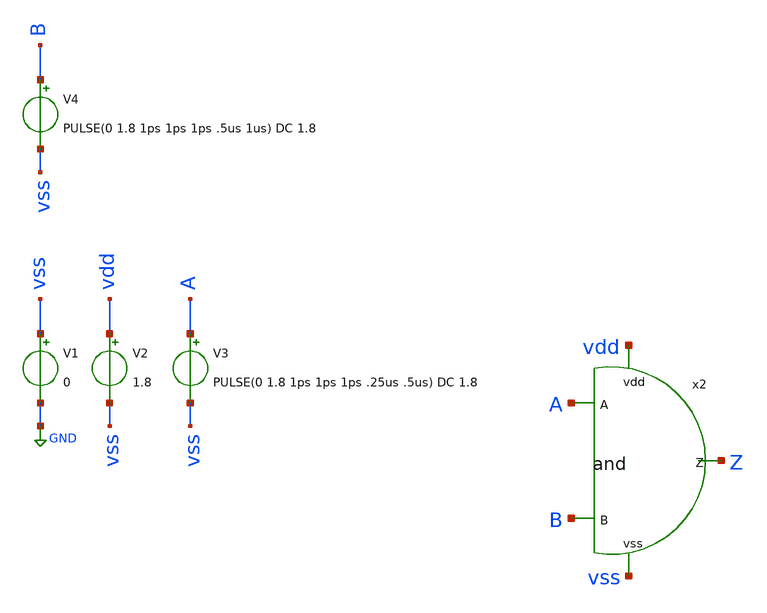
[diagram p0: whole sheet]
** sch_path: track_vlsi/somoza/sch/tb_and.sch
**.subckt tb_and
V1 vss GND 0
V2 vdd vss 1.8
V3 A vss PULSE(0 1.8 1ps 1ps 1ps .25us .5us) DC 1.8
V4 B vss PULSE(0 1.8 1ps 1ps 1ps .5us 1us) DC 1.8
x2 vdd A Z B vss and
**** begin user architecture code



* Parametros del circuito

.options TEMP = 27.0

* Include
.lib /home/eamta/skywater/skywater-pdk/libraries/sky130_fd_pr_ngspice/latest/models/corners/sky130.lib TT

* Signals to SAVE
*.save all
*+ @M.x1.XM1.msky130_fd_pr__nfet_01v8[id] @M.x1.XM1.msky130_fd_pr__nfet_01v8[gm]
*+ @M.x1.XM2.msky130_fd_pr__pfet_01v8[id] @M.x1.XM2.msky130_fd_pr__pfet_01v8[gm]

* Simulation
.control
  tran .001u 1us
  setplot tran1
  plot v(A)
  plot v(B)
  plot v(Z)
  write tb_and_tran.raw

.endc

.end


**** end user architecture code
**.ends

* expanding   symbol:  and/and.sym # of pins=5
** sym_path: track_vlsi/somoza/sch/and.sym
** sch_path: track_vlsi/somoza/sch/and.sch
.subckt and vdd A Z B vss
*.ipin A
*.ipin B
*.ipin vdd
*.opin Z
*.ipin vss
XM2 net1 A net2 vss sky130_fd_pr__nfet_01v8 L=0.15 W=0.9 nf=1 ad='int((nf+1)/2) * W/nf * 0.29' as='int((nf+2)/2) * W/nf * 0.29'
+ pd='2*int((nf+1)/2) * (W/nf + 0.29)' ps='2*int((nf+2)/2) * (W/nf + 0.29)' nrd='0.29 / W' nrs='0.29 / W'
+ sa=0 sb=0 sd=0 mult=1 m=1
XM3 net2 B vss vss sky130_fd_pr__nfet_01v8 L=0.15 W=0.9 nf=1 ad='int((nf+1)/2) * W/nf * 0.29' as='int((nf+2)/2) * W/nf * 0.29'
+ pd='2*int((nf+1)/2) * (W/nf + 0.29)' ps='2*int((nf+2)/2) * (W/nf + 0.29)' nrd='0.29 / W' nrs='0.29 / W'
+ sa=0 sb=0 sd=0 mult=1 m=1
XM1 net1 A vdd vdd sky130_fd_pr__pfet_01v8 L=0.15 W=0.9 nf=1 ad='int((nf+1)/2) * W/nf * 0.29' as='int((nf+2)/2) * W/nf * 0.29'
+ pd='2*int((nf+1)/2) * (W/nf + 0.29)' ps='2*int((nf+2)/2) * (W/nf + 0.29)' nrd='0.29 / W' nrs='0.29 / W'
+ sa=0 sb=0 sd=0 mult=1 m=1
XM0 net1 B vdd vdd sky130_fd_pr__pfet_01v8 L=0.15 W=0.9 nf=1 ad='int((nf+1)/2) * W/nf * 0.29' as='int((nf+2)/2) * W/nf * 0.29'
+ pd='2*int((nf+1)/2) * (W/nf + 0.29)' ps='2*int((nf+2)/2) * (W/nf + 0.29)' nrd='0.29 / W' nrs='0.29 / W'
+ sa=0 sb=0 sd=0 mult=1 m=1
XM4 Z net1 vdd vdd sky130_fd_pr__pfet_01v8 L=0.15 W=0.9 nf=1 ad='int((nf+1)/2) * W/nf * 0.29' as='int((nf+2)/2) * W/nf * 0.29'
+ pd='2*int((nf+1)/2) * (W/nf + 0.29)' ps='2*int((nf+2)/2) * (W/nf + 0.29)' nrd='0.29 / W' nrs='0.29 / W'
+ sa=0 sb=0 sd=0 mult=1 m=1
XM5 Z net1 vss vss sky130_fd_pr__nfet_01v8 L=0.15 W=0.45 nf=1 ad='int((nf+1)/2) * W/nf * 0.29' as='int((nf+2)/2) * W/nf * 0.29'
+ pd='2*int((nf+1)/2) * (W/nf + 0.29)' ps='2*int((nf+2)/2) * (W/nf + 0.29)' nrd='0.29 / W' nrs='0.29 / W'
+ sa=0 sb=0 sd=0 mult=1 m=1
.ends

.GLOBAL GND
.end
